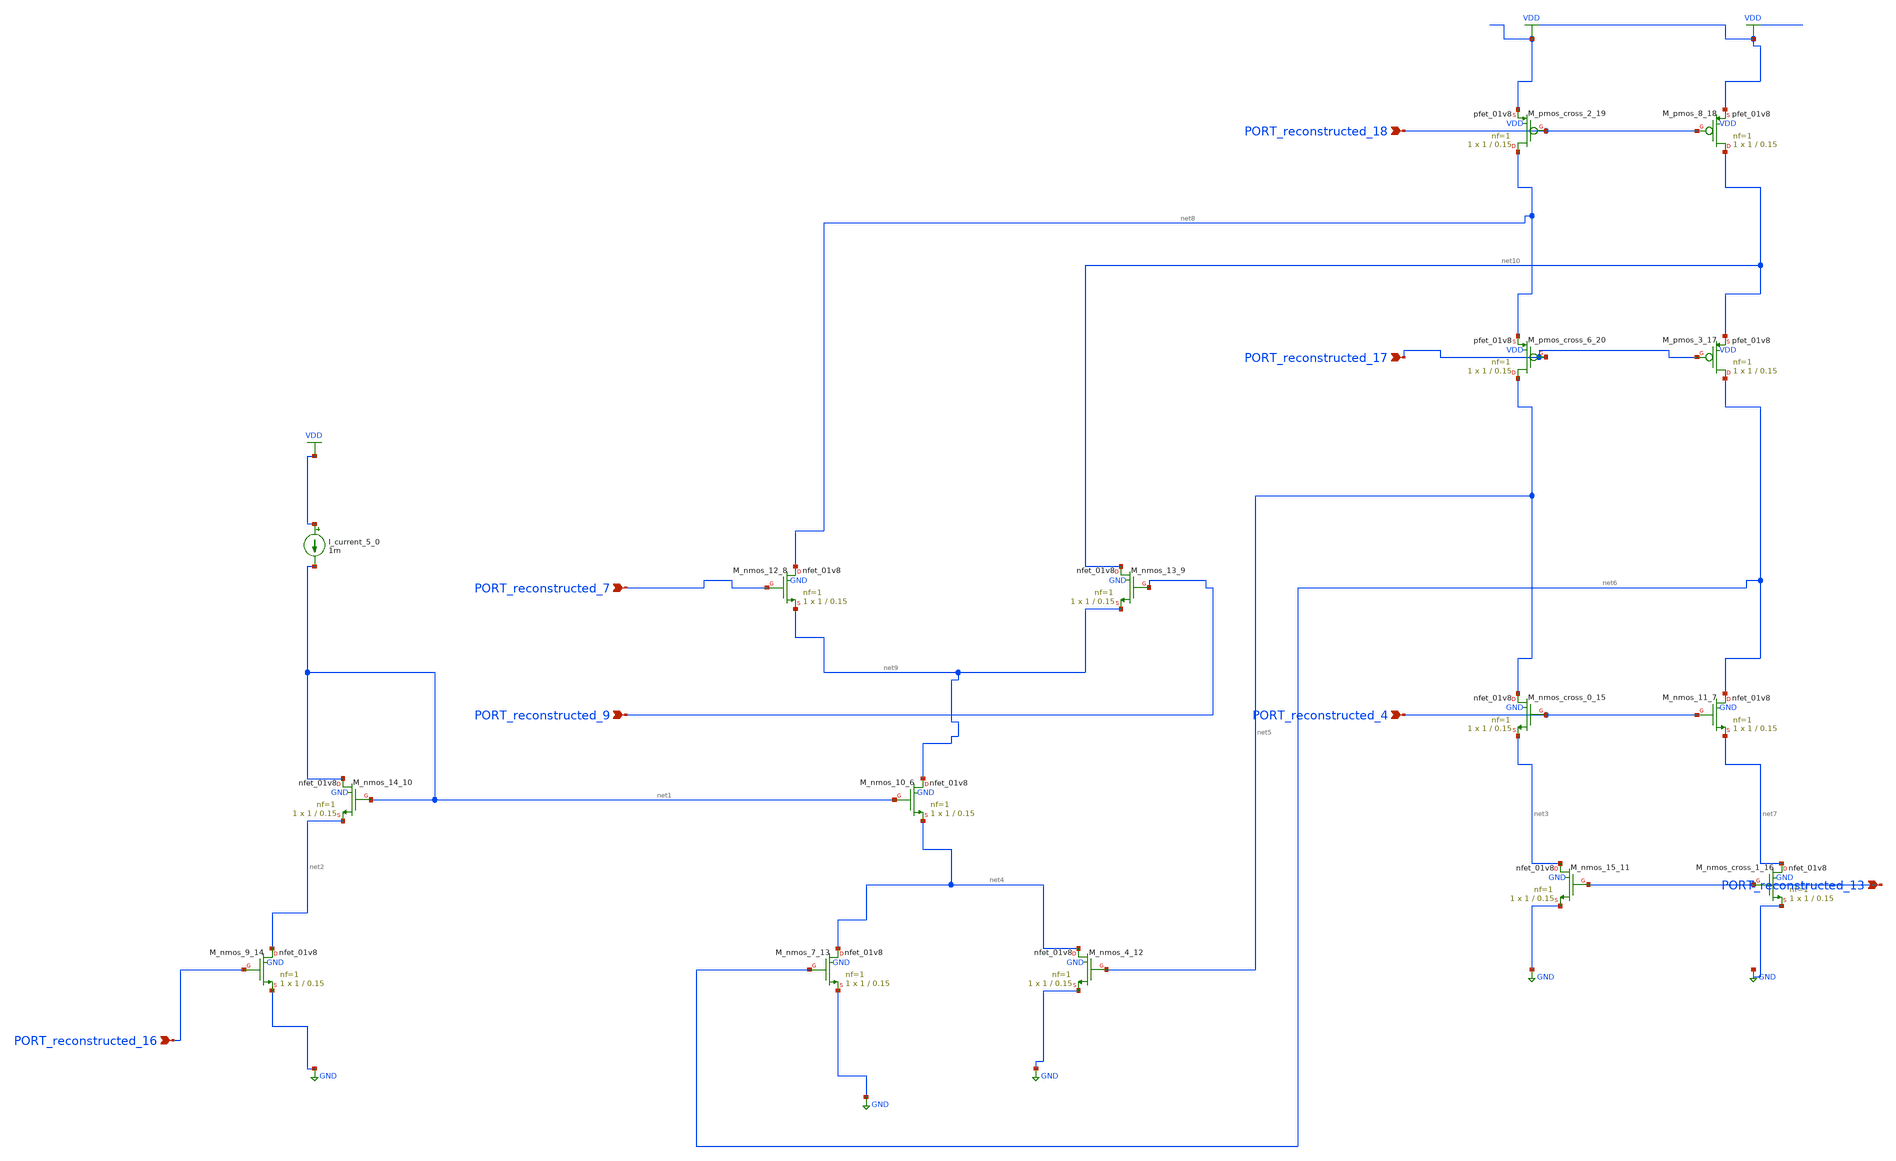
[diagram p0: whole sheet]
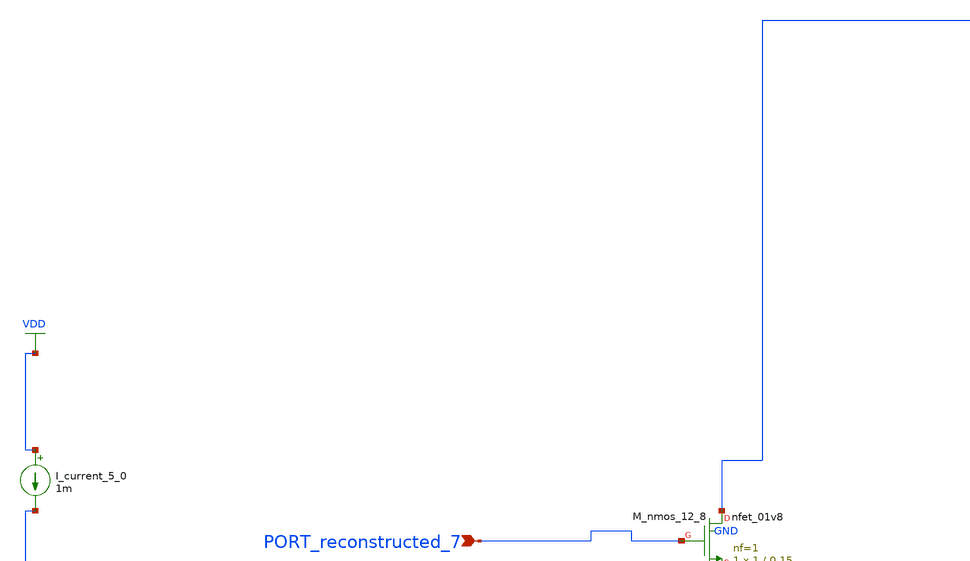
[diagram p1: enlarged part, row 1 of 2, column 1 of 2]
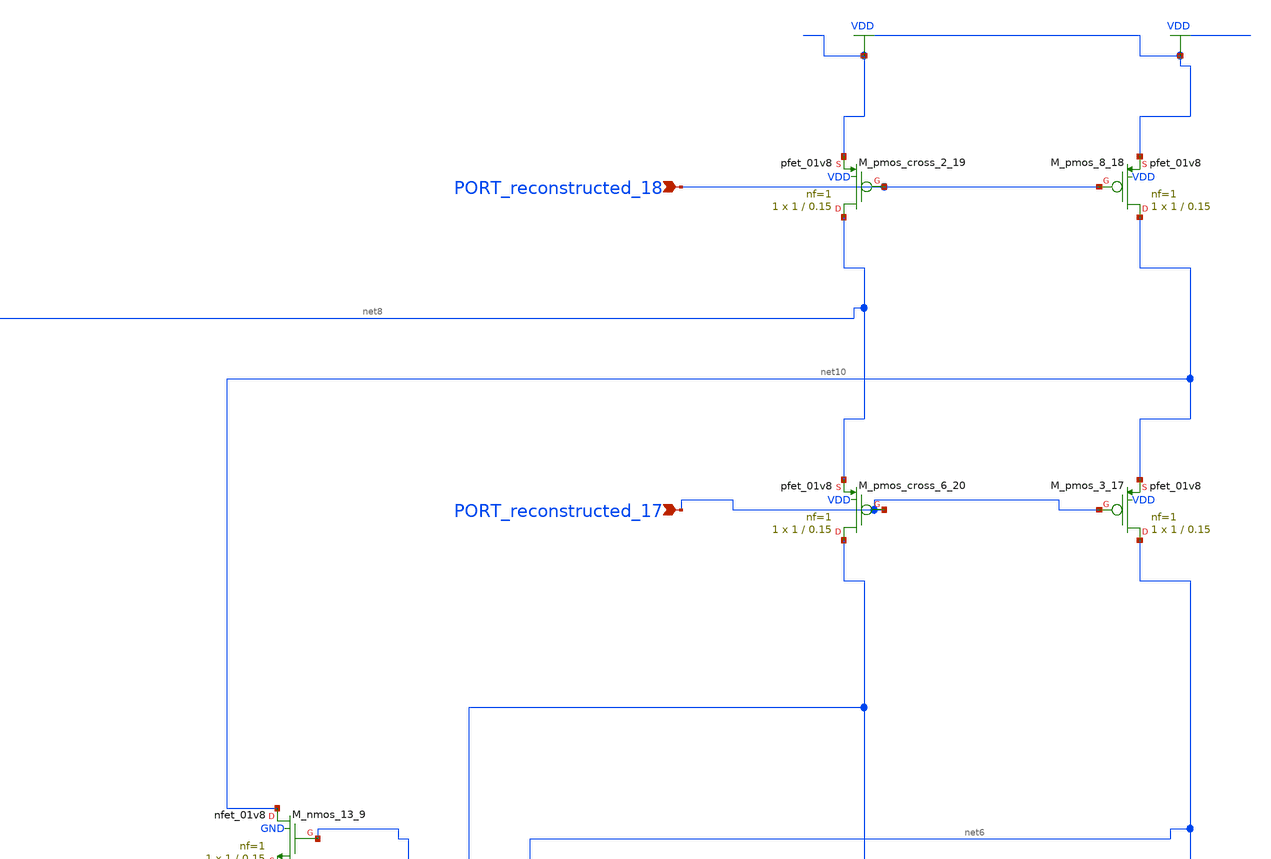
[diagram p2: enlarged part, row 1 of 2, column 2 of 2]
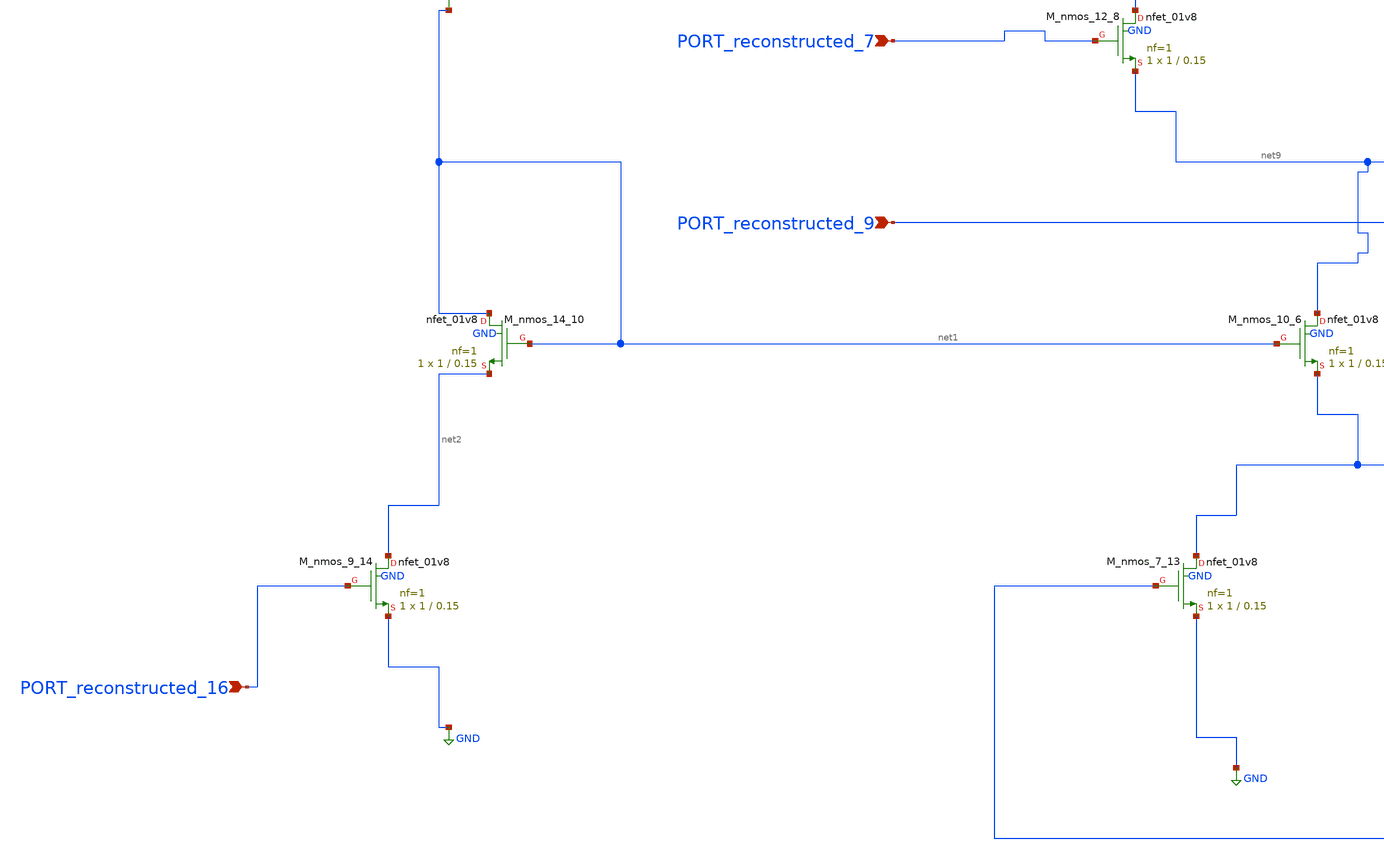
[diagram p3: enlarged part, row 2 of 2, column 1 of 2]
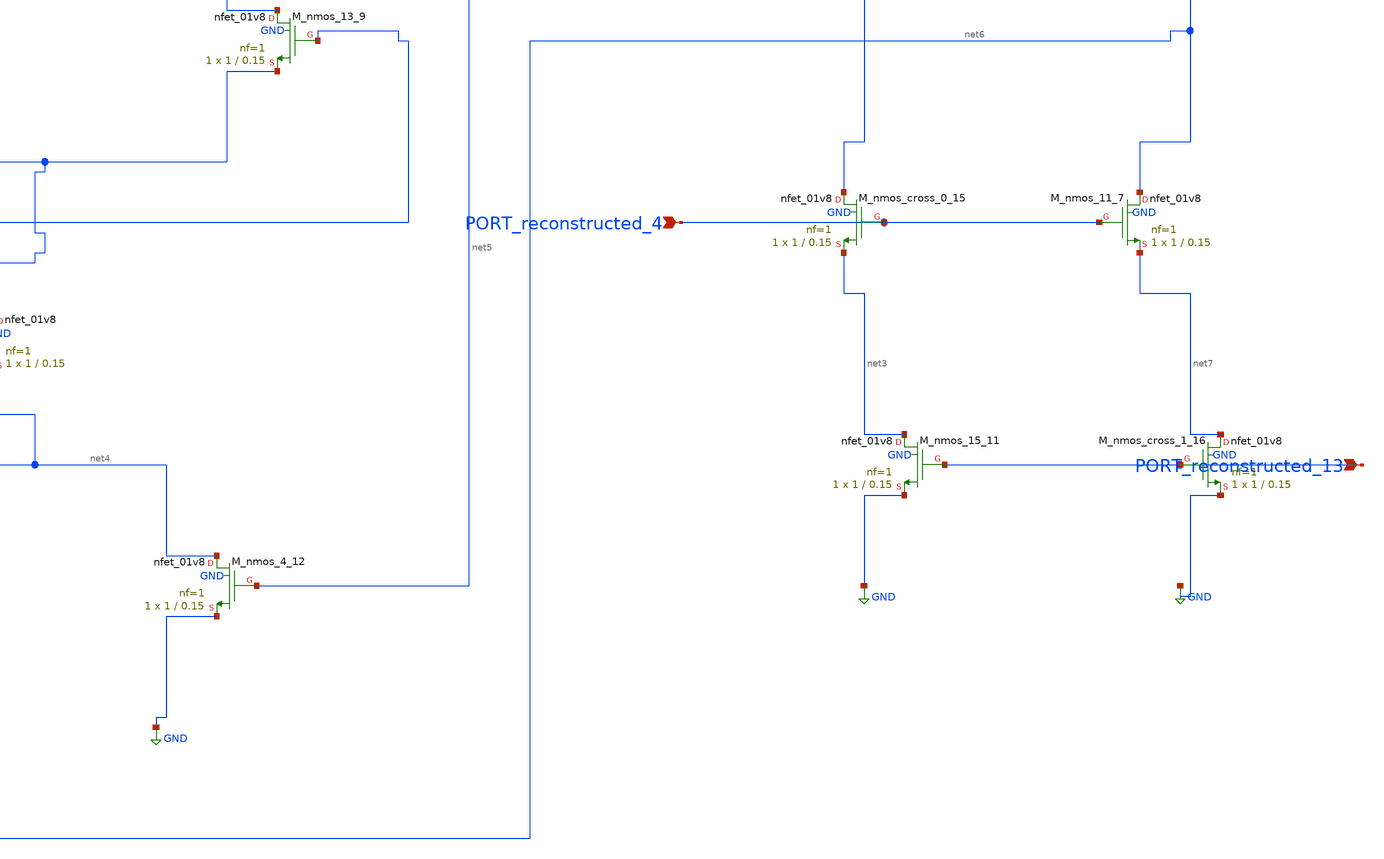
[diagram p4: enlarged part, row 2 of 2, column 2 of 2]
** sch_path: schematics/AMSNet/671.sch
**.subckt 671 PORT_reconstructed_7 PORT_reconstructed_9 PORT_reconstructed_16 PORT_reconstructed_13
*+ PORT_reconstructed_4 PORT_reconstructed_17 PORT_reconstructed_18
*.ipin PORT_reconstructed_7
*.ipin PORT_reconstructed_9
*.ipin PORT_reconstructed_16
*.ipin PORT_reconstructed_13
*.ipin PORT_reconstructed_4
*.ipin PORT_reconstructed_17
*.ipin PORT_reconstructed_18
I_current_5_0 VDD net1 1m
XM_nmos_10_6 net9 net1 net4 GND sky130_fd_pr__nfet_01v8 L=0.15 W=1 nf=1 ad='int((1 + 1)/2) * 1 / 1 * 0.29'
+ as='int((1 + 2)/2) * 1 / 1 * 0.29' pd='2*int((1 + 1)/2) * (1 / 1 + 0.29)' ps='2*int((1 + 2)/2) * (1 / 1 + 0.29)'
+ nrd='0.29 / 1 ' nrs='0.29 / 1 ' sa=0 sb=0 sd=0 mult=1 m=1
XM_nmos_11_7 net6 PORT_reconstructed_4 net7 GND sky130_fd_pr__nfet_01v8 L=0.15 W=1 nf=1 ad='int((1 + 1)/2) * 1 / 1 * 0.29'
+ as='int((1 + 2)/2) * 1 / 1 * 0.29' pd='2*int((1 + 1)/2) * (1 / 1 + 0.29)' ps='2*int((1 + 2)/2) * (1 / 1 + 0.29)'
+ nrd='0.29 / 1 ' nrs='0.29 / 1 ' sa=0 sb=0 sd=0 mult=1 m=1
XM_nmos_12_8 net8 PORT_reconstructed_7 net9 GND sky130_fd_pr__nfet_01v8 L=0.15 W=1 nf=1 ad='int((1 + 1)/2) * 1 / 1 * 0.29'
+ as='int((1 + 2)/2) * 1 / 1 * 0.29' pd='2*int((1 + 1)/2) * (1 / 1 + 0.29)' ps='2*int((1 + 2)/2) * (1 / 1 + 0.29)'
+ nrd='0.29 / 1 ' nrs='0.29 / 1 ' sa=0 sb=0 sd=0 mult=1 m=1
XM_nmos_13_9 net10 PORT_reconstructed_9 net9 GND sky130_fd_pr__nfet_01v8 L=0.15 W=1 nf=1 ad='int((1 + 1)/2) * 1 / 1 * 0.29'
+ as='int((1 + 2)/2) * 1 / 1 * 0.29' pd='2*int((1 + 1)/2) * (1 / 1 + 0.29)' ps='2*int((1 + 2)/2) * (1 / 1 + 0.29)'
+ nrd='0.29 / 1 ' nrs='0.29 / 1 ' sa=0 sb=0 sd=0 mult=1 m=1
XM_nmos_14_10 net1 net1 net2 GND sky130_fd_pr__nfet_01v8 L=0.15 W=1 nf=1 ad='int((1 + 1)/2) * 1 / 1 * 0.29'
+ as='int((1 + 2)/2) * 1 / 1 * 0.29' pd='2*int((1 + 1)/2) * (1 / 1 + 0.29)' ps='2*int((1 + 2)/2) * (1 / 1 + 0.29)'
+ nrd='0.29 / 1 ' nrs='0.29 / 1 ' sa=0 sb=0 sd=0 mult=1 m=1
XM_nmos_15_11 net3 PORT_reconstructed_13 GND GND sky130_fd_pr__nfet_01v8 L=0.15 W=1 nf=1 ad='int((1 + 1)/2) * 1 / 1 * 0.29'
+ as='int((1 + 2)/2) * 1 / 1 * 0.29' pd='2*int((1 + 1)/2) * (1 / 1 + 0.29)' ps='2*int((1 + 2)/2) * (1 / 1 + 0.29)'
+ nrd='0.29 / 1 ' nrs='0.29 / 1 ' sa=0 sb=0 sd=0 mult=1 m=1
XM_nmos_4_12 net4 net5 GND GND sky130_fd_pr__nfet_01v8 L=0.15 W=1 nf=1 ad='int((1 + 1)/2) * 1 / 1 * 0.29'
+ as='int((1 + 2)/2) * 1 / 1 * 0.29' pd='2*int((1 + 1)/2) * (1 / 1 + 0.29)' ps='2*int((1 + 2)/2) * (1 / 1 + 0.29)'
+ nrd='0.29 / 1 ' nrs='0.29 / 1 ' sa=0 sb=0 sd=0 mult=1 m=1
XM_nmos_7_13 net4 net6 GND GND sky130_fd_pr__nfet_01v8 L=0.15 W=1 nf=1 ad='int((1 + 1)/2) * 1 / 1 * 0.29'
+ as='int((1 + 2)/2) * 1 / 1 * 0.29' pd='2*int((1 + 1)/2) * (1 / 1 + 0.29)' ps='2*int((1 + 2)/2) * (1 / 1 + 0.29)'
+ nrd='0.29 / 1 ' nrs='0.29 / 1 ' sa=0 sb=0 sd=0 mult=1 m=1
XM_nmos_9_14 net2 PORT_reconstructed_16 GND GND sky130_fd_pr__nfet_01v8 L=0.15 W=1 nf=1 ad='int((1 + 1)/2) * 1 / 1 * 0.29'
+ as='int((1 + 2)/2) * 1 / 1 * 0.29' pd='2*int((1 + 1)/2) * (1 / 1 + 0.29)' ps='2*int((1 + 2)/2) * (1 / 1 + 0.29)'
+ nrd='0.29 / 1 ' nrs='0.29 / 1 ' sa=0 sb=0 sd=0 mult=1 m=1
XM_nmos_cross_0_15 net5 PORT_reconstructed_4 net3 GND sky130_fd_pr__nfet_01v8 L=0.15 W=1 nf=1 ad='int((1 + 1)/2) * 1 / 1 * 0.29'
+ as='int((1 + 2)/2) * 1 / 1 * 0.29' pd='2*int((1 + 1)/2) * (1 / 1 + 0.29)' ps='2*int((1 + 2)/2) * (1 / 1 + 0.29)'
+ nrd='0.29 / 1 ' nrs='0.29 / 1 ' sa=0 sb=0 sd=0 mult=1 m=1
XM_nmos_cross_1_16 net7 PORT_reconstructed_13 GND GND sky130_fd_pr__nfet_01v8 L=0.15 W=1 nf=1 ad='int((1 + 1)/2) * 1 / 1 * 0.29'
+ as='int((1 + 2)/2) * 1 / 1 * 0.29' pd='2*int((1 + 1)/2) * (1 / 1 + 0.29)' ps='2*int((1 + 2)/2) * (1 / 1 + 0.29)'
+ nrd='0.29 / 1 ' nrs='0.29 / 1 ' sa=0 sb=0 sd=0 mult=1 m=1
XM_pmos_3_17 net6 PORT_reconstructed_17 net10 VDD sky130_fd_pr__pfet_01v8 L=0.15 W=1 nf=1 ad='int((1 + 1)/2) * 1 / 1 * 0.29'
+ as='int((1 + 2)/2) * 1 / 1 * 0.29' pd='2*int((1 + 1)/2) * (1 / 1 + 0.29)' ps='2*int((1 + 2)/2) * (1 / 1 + 0.29)'
+ nrd='0.29 / 1 ' nrs='0.29 / 1 ' sa=0 sb=0 sd=0 mult=1 m=1
XM_pmos_8_18 net10 PORT_reconstructed_18 VDD VDD sky130_fd_pr__pfet_01v8 L=0.15 W=1 nf=1 ad='int((1 + 1)/2) * 1 / 1 * 0.29'
+ as='int((1 + 2)/2) * 1 / 1 * 0.29' pd='2*int((1 + 1)/2) * (1 / 1 + 0.29)' ps='2*int((1 + 2)/2) * (1 / 1 + 0.29)'
+ nrd='0.29 / 1 ' nrs='0.29 / 1 ' sa=0 sb=0 sd=0 mult=1 m=1
XM_pmos_cross_2_19 net8 PORT_reconstructed_18 VDD VDD sky130_fd_pr__pfet_01v8 L=0.15 W=1 nf=1 ad='int((1 + 1)/2) * 1 / 1 * 0.29'
+ as='int((1 + 2)/2) * 1 / 1 * 0.29' pd='2*int((1 + 1)/2) * (1 / 1 + 0.29)' ps='2*int((1 + 2)/2) * (1 / 1 + 0.29)'
+ nrd='0.29 / 1 ' nrs='0.29 / 1 ' sa=0 sb=0 sd=0 mult=1 m=1
XM_pmos_cross_6_20 net5 PORT_reconstructed_17 net8 VDD sky130_fd_pr__pfet_01v8 L=0.15 W=1 nf=1 ad='int((1 + 1)/2) * 1 / 1 * 0.29'
+ as='int((1 + 2)/2) * 1 / 1 * 0.29' pd='2*int((1 + 1)/2) * (1 / 1 + 0.29)' ps='2*int((1 + 2)/2) * (1 / 1 + 0.29)'
+ nrd='0.29 / 1 ' nrs='0.29 / 1 ' sa=0 sb=0 sd=0 mult=1 m=1
**.ends
.GLOBAL GND
.GLOBAL VDD
.end
